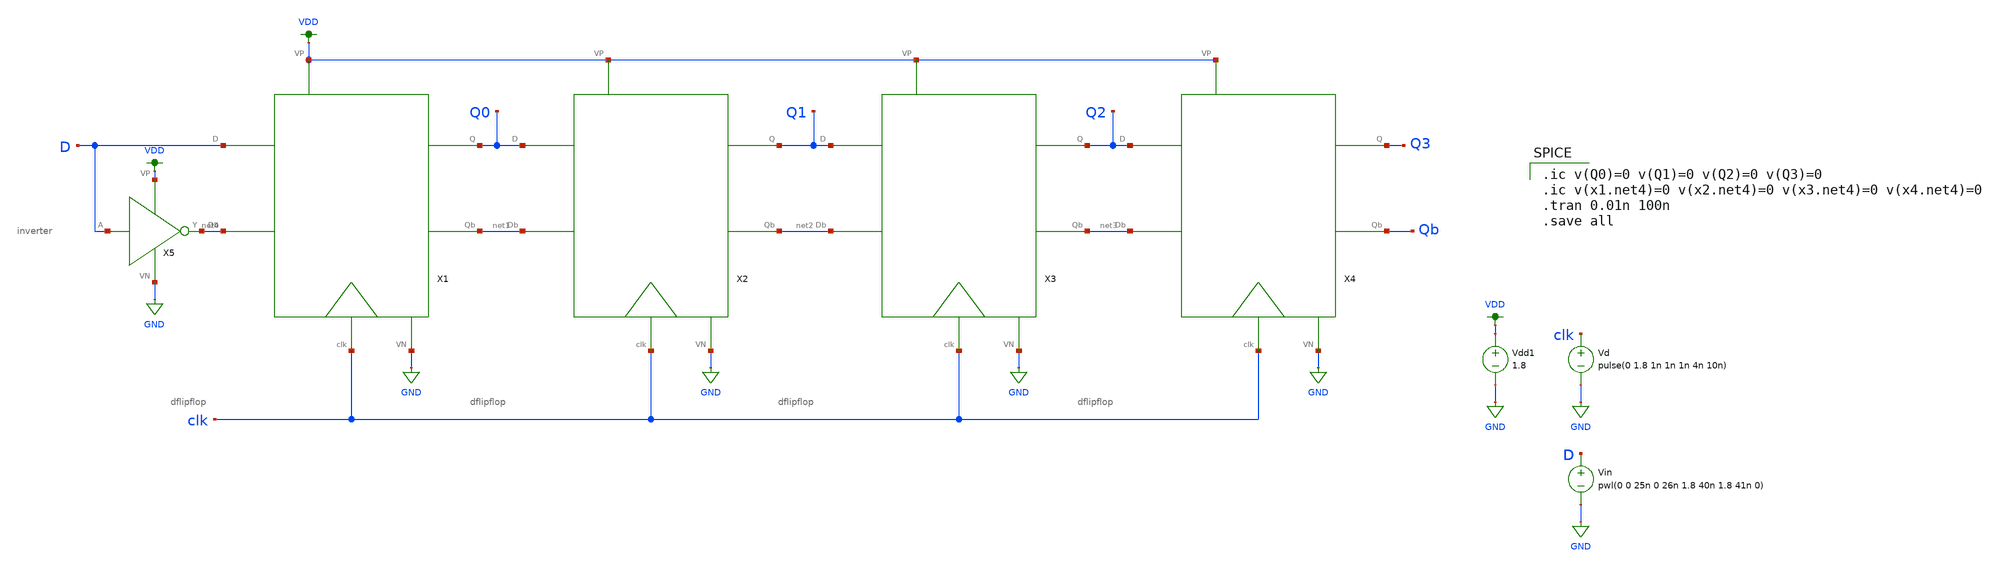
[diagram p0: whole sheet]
** sch_path: Miniproject2/shift_reg_trans.sch
**.subckt shift_reg_trans
X1 VDD Q0 net1 GND clk net4 D dflipflop
X2 VDD Q1 net2 GND clk net1 Q0 dflipflop
X3 VDD Q2 net3 GND clk net2 Q1 dflipflop
X4 VDD Q3 Qb GND clk net3 Q2 dflipflop
X5 D net4 VDD GND inverter
Vdd1 VDD GND 1.8
Vin D GND pwl(0 0 25n 0 26n 1.8 40n 1.8 41n 0)
Vd clk GND pulse(0 1.8 1n 1n 1n 4n 10n)
**** begin user architecture code

.option wnflag=1
.lib ~/skywater/skywater-pdk/libraries/sky130_fd_pr_ngspice/latest/models/sky130.lib.spice tt


.ic v(Q0)=0 v(Q1)=0 v(Q2)=0 v(Q3)=0
.ic v(x1.net4)=0 v(x2.net4)=0 v(x3.net4)=0 v(x4.net4)=0
.tran 0.01n 100n
.save all

**** end user architecture code
**.ends
.GLOBAL VDD
.GLOBAL GND
.end
